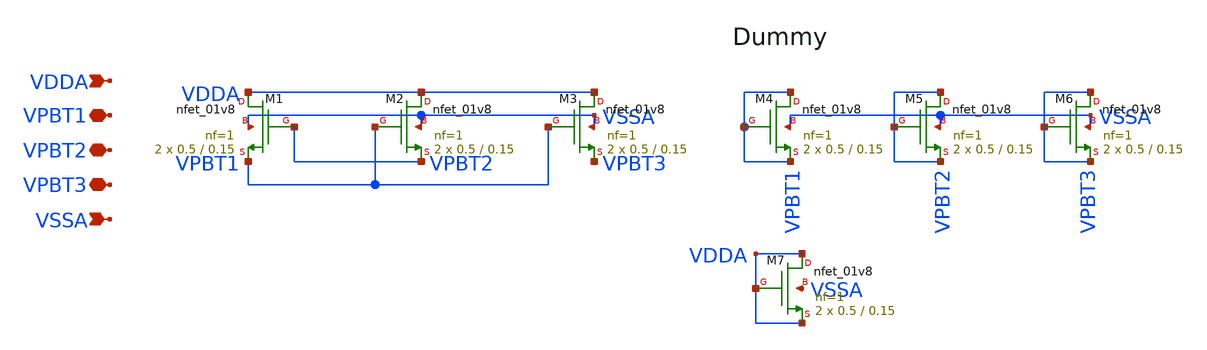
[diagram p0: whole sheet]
** sch_path: xschem/ncell_bsw.sch
**.subckt ncell_bsw VDDA VPBT1 VPBT2 VPBT3 VSSA
*.ipin VDDA
*.iopin VPBT1
*.iopin VPBT2
*.iopin VPBT3
*.ipin VSSA
XM1 VDDA VPBT2 VPBT1 VSSA sky130_fd_pr__nfet_01v8 L=0.15 W=0.5 nf=1 ad='int((nf+1)/2) * W/nf * 0.29'
+ as='int((nf+2)/2) * W/nf * 0.29' pd='2*int((nf+1)/2) * (W/nf + 0.29)' ps='2*int((nf+2)/2) * (W/nf + 0.29)'
+ nrd='0.29 / W' nrs='0.29 / W' sa=0 sb=0 sd=0 mult=2 m=2
XM2 VDDA VPBT1 VPBT2 VSSA sky130_fd_pr__nfet_01v8 L=0.15 W=0.5 nf=1 ad='int((nf+1)/2) * W/nf * 0.29'
+ as='int((nf+2)/2) * W/nf * 0.29' pd='2*int((nf+1)/2) * (W/nf + 0.29)' ps='2*int((nf+2)/2) * (W/nf + 0.29)'
+ nrd='0.29 / W' nrs='0.29 / W' sa=0 sb=0 sd=0 mult=2 m=2
XM3 VDDA VPBT1 VPBT3 VSSA sky130_fd_pr__nfet_01v8 L=0.15 W=0.5 nf=1 ad='int((nf+1)/2) * W/nf * 0.29'
+ as='int((nf+2)/2) * W/nf * 0.29' pd='2*int((nf+1)/2) * (W/nf + 0.29)' ps='2*int((nf+2)/2) * (W/nf + 0.29)'
+ nrd='0.29 / W' nrs='0.29 / W' sa=0 sb=0 sd=0 mult=2 m=2
XM4 VPBT1 VPBT1 VPBT1 VSSA sky130_fd_pr__nfet_01v8 L=0.15 W=0.5 nf=1 ad='int((nf+1)/2) * W/nf * 0.29'
+ as='int((nf+2)/2) * W/nf * 0.29' pd='2*int((nf+1)/2) * (W/nf + 0.29)' ps='2*int((nf+2)/2) * (W/nf + 0.29)'
+ nrd='0.29 / W' nrs='0.29 / W' sa=0 sb=0 sd=0 mult=2 m=2
XM5 VPBT2 VPBT2 VPBT2 VSSA sky130_fd_pr__nfet_01v8 L=0.15 W=0.5 nf=1 ad='int((nf+1)/2) * W/nf * 0.29'
+ as='int((nf+2)/2) * W/nf * 0.29' pd='2*int((nf+1)/2) * (W/nf + 0.29)' ps='2*int((nf+2)/2) * (W/nf + 0.29)'
+ nrd='0.29 / W' nrs='0.29 / W' sa=0 sb=0 sd=0 mult=2 m=2
XM6 VPBT3 VPBT3 VPBT3 VSSA sky130_fd_pr__nfet_01v8 L=0.15 W=0.5 nf=1 ad='int((nf+1)/2) * W/nf * 0.29'
+ as='int((nf+2)/2) * W/nf * 0.29' pd='2*int((nf+1)/2) * (W/nf + 0.29)' ps='2*int((nf+2)/2) * (W/nf + 0.29)'
+ nrd='0.29 / W' nrs='0.29 / W' sa=0 sb=0 sd=0 mult=2 m=2
XM7 VDDA VDDA VDDA VSSA sky130_fd_pr__nfet_01v8 L=0.15 W=0.5 nf=1 ad='int((nf+1)/2) * W/nf * 0.29' as='int((nf+2)/2) * W/nf * 0.29'
+ pd='2*int((nf+1)/2) * (W/nf + 0.29)' ps='2*int((nf+2)/2) * (W/nf + 0.29)' nrd='0.29 / W' nrs='0.29 / W'
+ sa=0 sb=0 sd=0 mult=2 m=2
**.ends
.end
